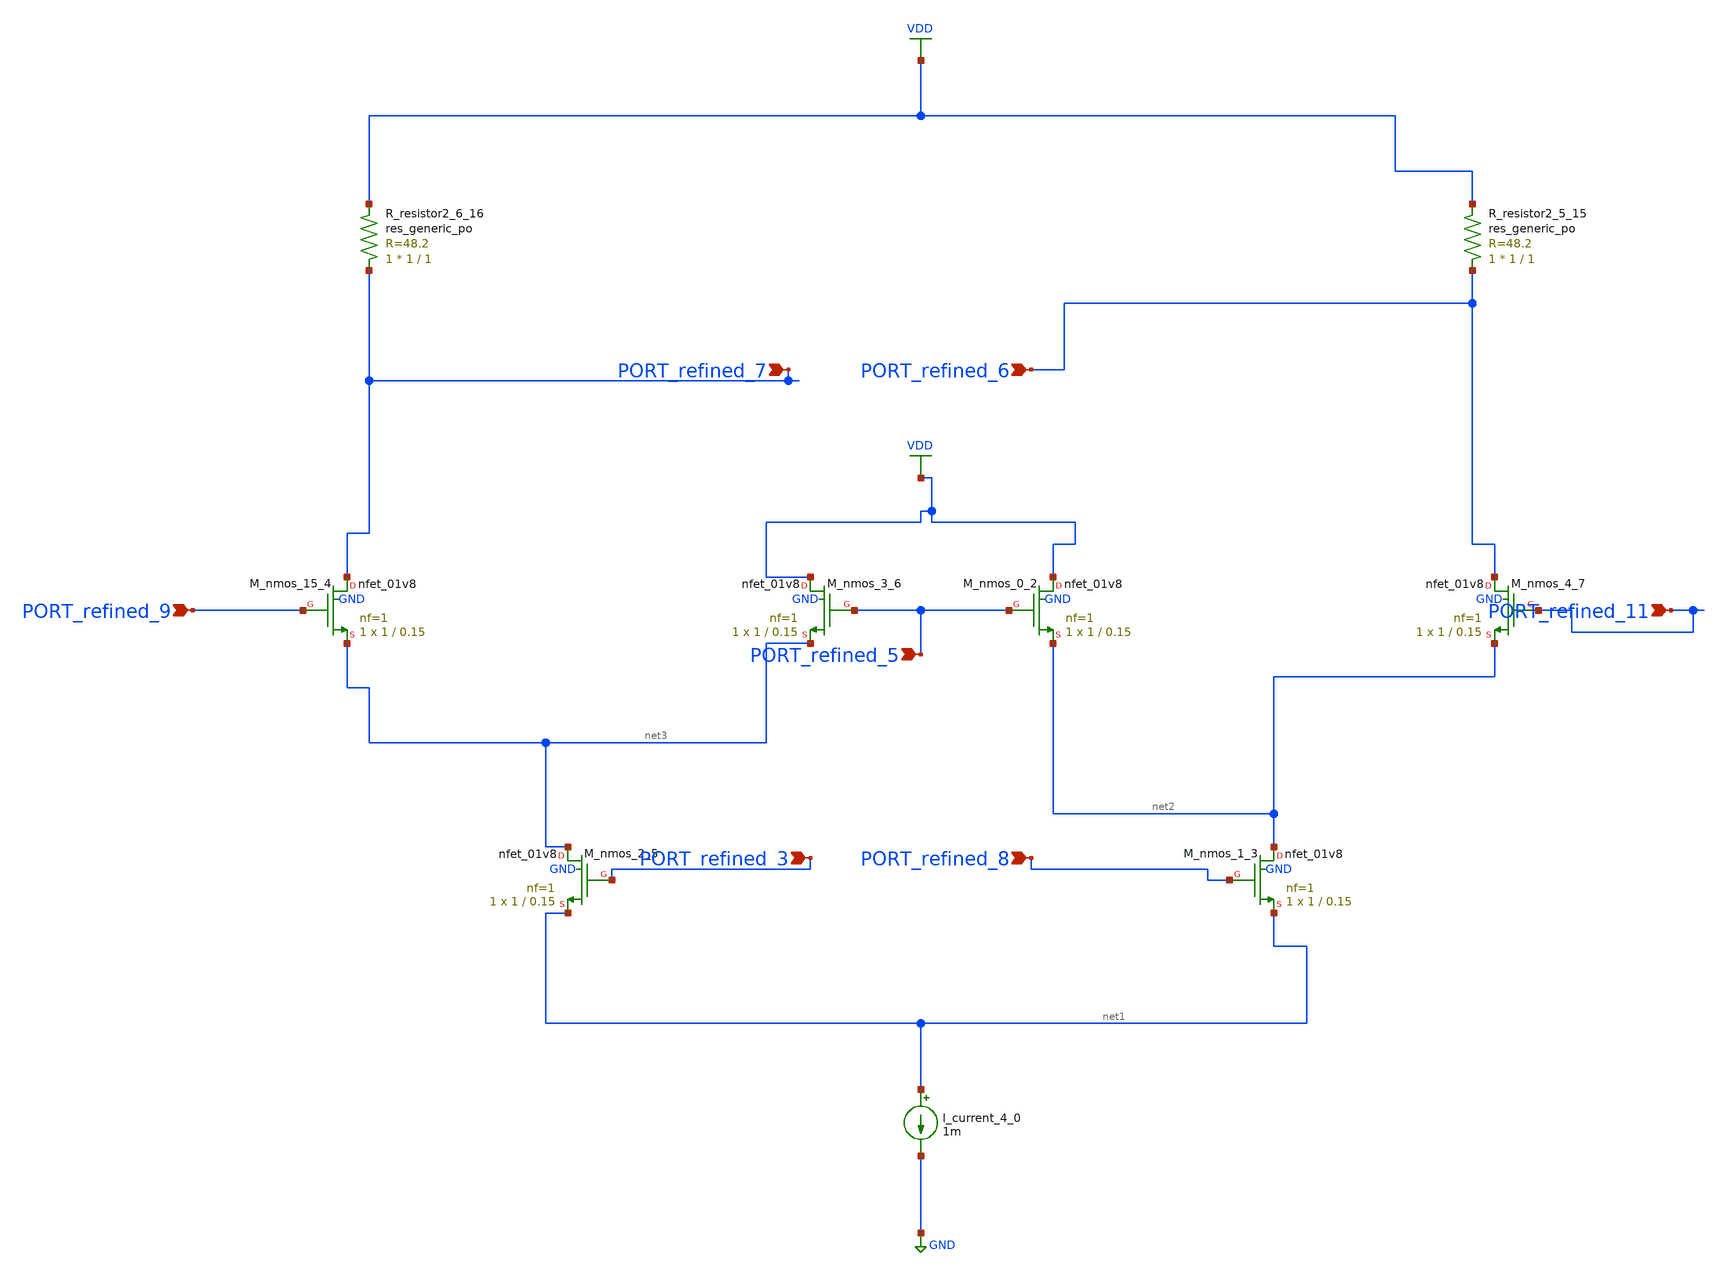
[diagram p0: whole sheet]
** sch_path: schematics/10_29292_jics_v17i1_583_03_003_crop2.sch
**.subckt 10_29292_jics_v17i1_583_03_003_crop2 PORT_refined_3 PORT_refined_6 PORT_refined_7
*+ PORT_refined_9 PORT_refined_11 PORT_refined_5 PORT_refined_8
*.ipin PORT_refined_3
*.ipin PORT_refined_6
*.ipin PORT_refined_7
*.ipin PORT_refined_9
*.ipin PORT_refined_11
*.ipin PORT_refined_5
*.ipin PORT_refined_8
I_current_4_0 net1 GND 1m
XM_nmos_0_2 VDD PORT_refined_5 net2 GND sky130_fd_pr__nfet_01v8 L=0.15 W=1 nf=1 ad='int((1 + 1)/2) * 1 / 1 * 0.29'
+ as='int((1 + 2)/2) * 1 / 1 * 0.29' pd='2*int((1 + 1)/2) * (1 / 1 + 0.29)' ps='2*int((1 + 2)/2) * (1 / 1 + 0.29)'
+ nrd='0.29 / 1 ' nrs='0.29 / 1 ' sa=0 sb=0 sd=0 mult=1 m=1
XM_nmos_1_3 net2 PORT_refined_8 net1 GND sky130_fd_pr__nfet_01v8 L=0.15 W=1 nf=1 ad='int((1 + 1)/2) * 1 / 1 * 0.29'
+ as='int((1 + 2)/2) * 1 / 1 * 0.29' pd='2*int((1 + 1)/2) * (1 / 1 + 0.29)' ps='2*int((1 + 2)/2) * (1 / 1 + 0.29)'
+ nrd='0.29 / 1 ' nrs='0.29 / 1 ' sa=0 sb=0 sd=0 mult=1 m=1
XM_nmos_15_4 PORT_refined_7 PORT_refined_9 net3 GND sky130_fd_pr__nfet_01v8 L=0.15 W=1 nf=1 ad='int((1 + 1)/2) * 1 / 1 * 0.29'
+ as='int((1 + 2)/2) * 1 / 1 * 0.29' pd='2*int((1 + 1)/2) * (1 / 1 + 0.29)' ps='2*int((1 + 2)/2) * (1 / 1 + 0.29)'
+ nrd='0.29 / 1 ' nrs='0.29 / 1 ' sa=0 sb=0 sd=0 mult=1 m=1
XM_nmos_2_5 net3 PORT_refined_3 net1 GND sky130_fd_pr__nfet_01v8 L=0.15 W=1 nf=1 ad='int((1 + 1)/2) * 1 / 1 * 0.29'
+ as='int((1 + 2)/2) * 1 / 1 * 0.29' pd='2*int((1 + 1)/2) * (1 / 1 + 0.29)' ps='2*int((1 + 2)/2) * (1 / 1 + 0.29)'
+ nrd='0.29 / 1 ' nrs='0.29 / 1 ' sa=0 sb=0 sd=0 mult=1 m=1
XM_nmos_3_6 VDD PORT_refined_5 net3 GND sky130_fd_pr__nfet_01v8 L=0.15 W=1 nf=1 ad='int((1 + 1)/2) * 1 / 1 * 0.29'
+ as='int((1 + 2)/2) * 1 / 1 * 0.29' pd='2*int((1 + 1)/2) * (1 / 1 + 0.29)' ps='2*int((1 + 2)/2) * (1 / 1 + 0.29)'
+ nrd='0.29 / 1 ' nrs='0.29 / 1 ' sa=0 sb=0 sd=0 mult=1 m=1
XM_nmos_4_7 PORT_refined_6 PORT_refined_11 net2 GND sky130_fd_pr__nfet_01v8 L=0.15 W=1 nf=1 ad='int((1 + 1)/2) * 1 / 1 * 0.29'
+ as='int((1 + 2)/2) * 1 / 1 * 0.29' pd='2*int((1 + 1)/2) * (1 / 1 + 0.29)' ps='2*int((1 + 2)/2) * (1 / 1 + 0.29)'
+ nrd='0.29 / 1 ' nrs='0.29 / 1 ' sa=0 sb=0 sd=0 mult=1 m=1
XR_resistor2_5_15 PORT_refined_6 VDD sky130_fd_pr__res_generic_po W=1 L=1 m=1
XR_resistor2_6_16 PORT_refined_7 VDD sky130_fd_pr__res_generic_po W=1 L=1 m=1
**.ends
.GLOBAL GND
.GLOBAL VDD
.end
